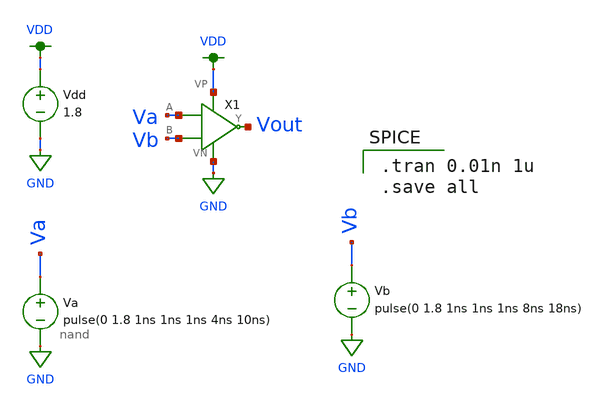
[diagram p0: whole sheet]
** sch_path: 1_And_Gate/nand_test.sch
**.subckt nand_test
Vdd VDD GND 1.8
Va Va GND pulse(0 1.8 1ns 1ns 1ns 4ns 10ns)
X1 Va Vout VDD GND Vb nand
Vb Vb GND pulse(0 1.8 1ns 1ns 1ns 8ns 18ns)
**** begin user architecture code

.tran 0.01n 1u
.save all


.option wnflag=1
.lib ~/skywater/skywater-pdk/libraries/sky130_fd_pr_ngspice/latest/models/sky130.lib.spice tt

**** end user architecture code
**.ends
.GLOBAL VDD
.GLOBAL GND
.end
